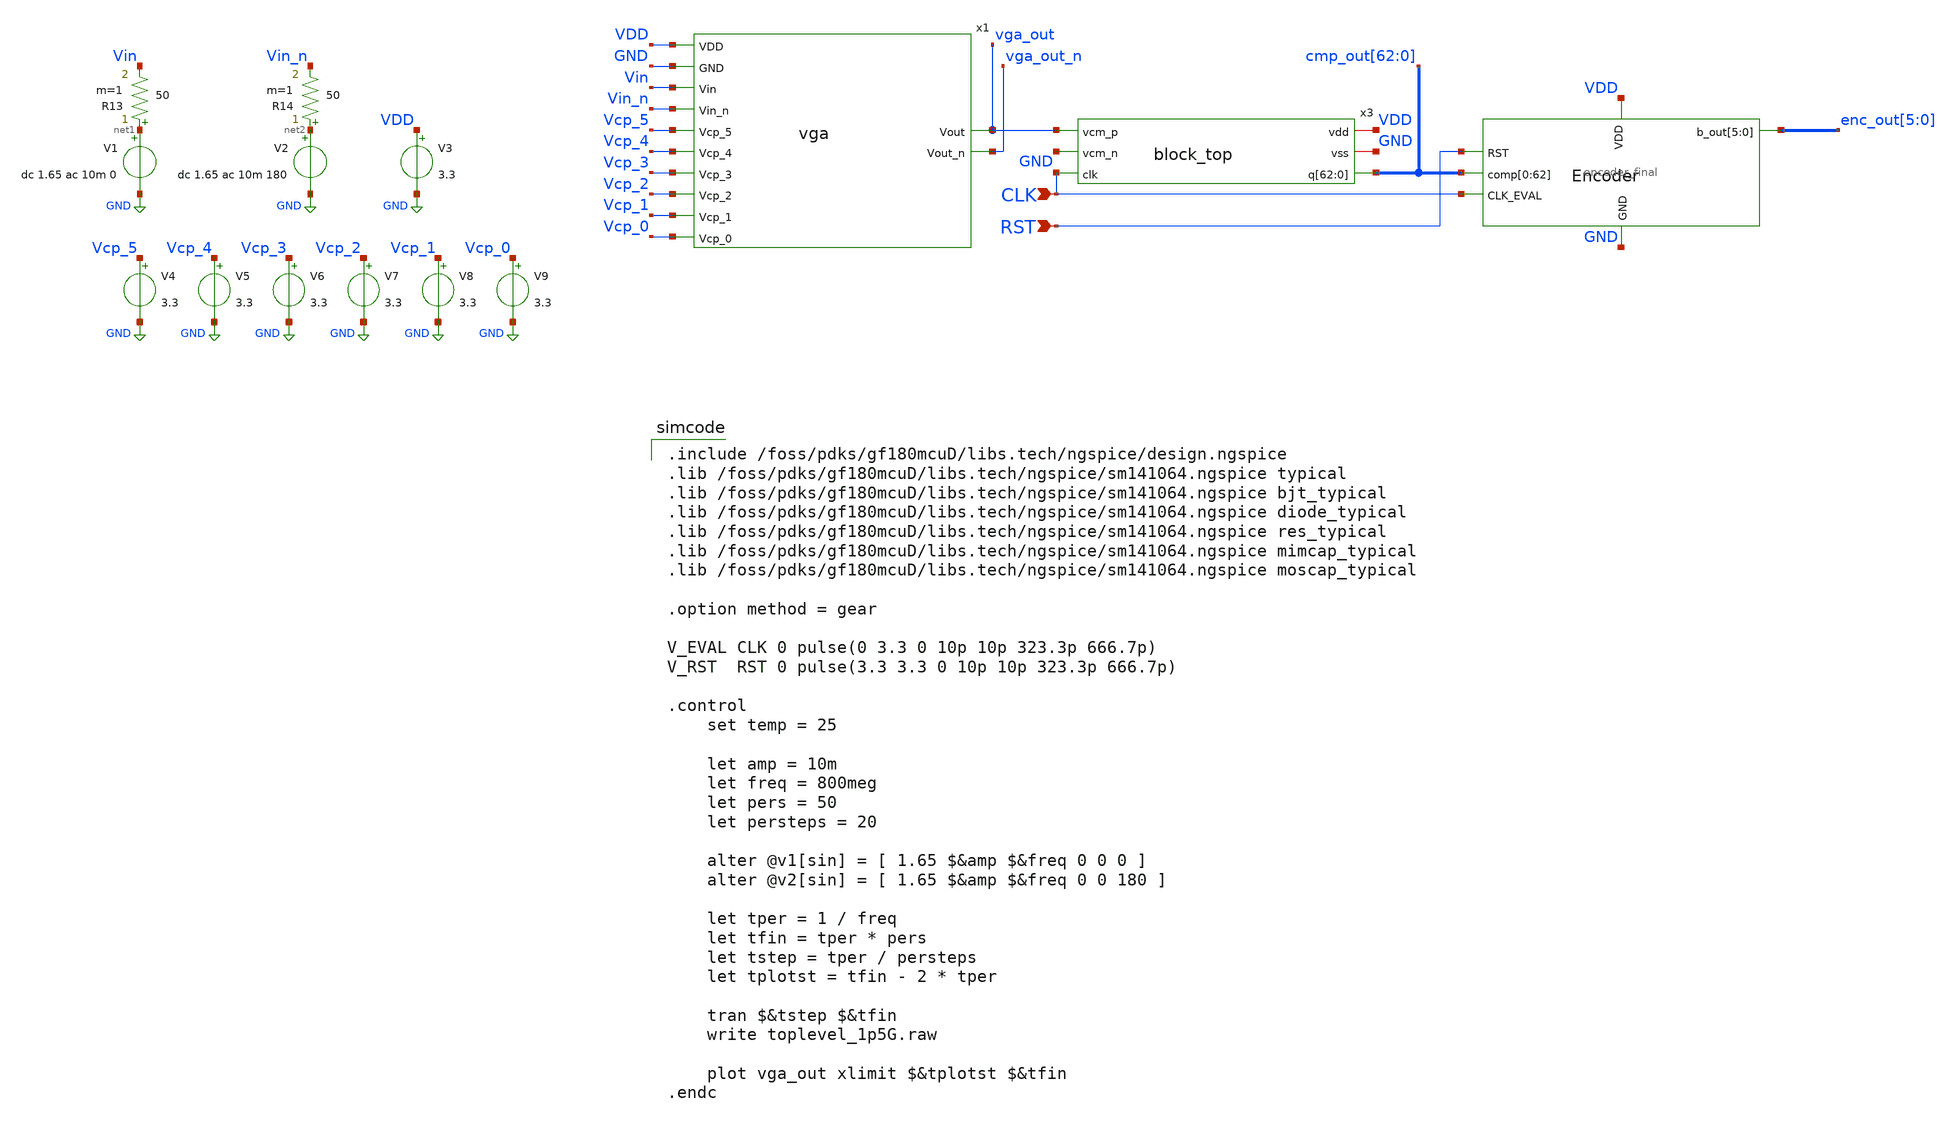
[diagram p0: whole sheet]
** sch_path: blocks/adc/adc_top.sch
**.subckt adc_top CLK RST
*.ipin CLK
*.ipin RST
x1 VDD vga_out Vcp_5 Vcp_4 Vin Vin_n Vcp_2 Vcp_3 Vcp_1 Vcp_0 GND vga_out_n vga
V1 net1 GND dc 1.65 ac 10m 0
V2 net2 GND dc 1.65 ac 10m 180
R14 net2 Vin_n 50 m=1
R13 net1 Vin 50 m=1
V3 VDD GND 3.3
V4 Vcp_5 GND 3.3
V5 Vcp_4 GND 3.3
V6 Vcp_3 GND 3.3
V7 Vcp_2 GND 3.3
V8 Vcp_1 GND 3.3
V9 Vcp_0 GND 3.3
x3 VDD GND vga_out GND CLK cmp_out[62] cmp_out[61] cmp_out[60] cmp_out[59] cmp_out[58] cmp_out[57]
+ cmp_out[56] cmp_out[55] cmp_out[54] cmp_out[53] cmp_out[52] cmp_out[51] cmp_out[50] cmp_out[49] cmp_out[48]
+ cmp_out[47] cmp_out[46] cmp_out[45] cmp_out[44] cmp_out[43] cmp_out[42] cmp_out[41] cmp_out[40] cmp_out[39]
+ cmp_out[38] cmp_out[37] cmp_out[36] cmp_out[35] cmp_out[34] cmp_out[33] cmp_out[32] cmp_out[31] cmp_out[30]
+ cmp_out[29] cmp_out[28] cmp_out[27] cmp_out[26] cmp_out[25] cmp_out[24] cmp_out[23] cmp_out[22] cmp_out[21]
+ cmp_out[20] cmp_out[19] cmp_out[18] cmp_out[17] cmp_out[16] cmp_out[15] cmp_out[14] cmp_out[13] cmp_out[12]
+ cmp_out[11] cmp_out[10] cmp_out[9] cmp_out[8] cmp_out[7] cmp_out[6] cmp_out[5] cmp_out[4] cmp_out[3] cmp_out[2]
+ cmp_out[1] cmp_out[0] block_top
x2 VDD enc_out[5] enc_out[4] enc_out[3] enc_out[2] enc_out[1] enc_out[0] RST cmp_out[62] cmp_out[61]
+ cmp_out[60] cmp_out[59] cmp_out[58] cmp_out[57] cmp_out[56] cmp_out[55] cmp_out[54] cmp_out[53] cmp_out[52]
+ cmp_out[51] cmp_out[50] cmp_out[49] cmp_out[48] cmp_out[47] cmp_out[46] cmp_out[45] cmp_out[44] cmp_out[43]
+ cmp_out[42] cmp_out[41] cmp_out[40] cmp_out[39] cmp_out[38] cmp_out[37] cmp_out[36] cmp_out[35] cmp_out[34]
+ cmp_out[33] cmp_out[32] cmp_out[31] cmp_out[30] cmp_out[29] cmp_out[28] cmp_out[27] cmp_out[26] cmp_out[25]
+ cmp_out[24] cmp_out[23] cmp_out[22] cmp_out[21] cmp_out[20] cmp_out[19] cmp_out[18] cmp_out[17] cmp_out[16]
+ cmp_out[15] cmp_out[14] cmp_out[13] cmp_out[12] cmp_out[11] cmp_out[10] cmp_out[9] cmp_out[8] cmp_out[7]
+ cmp_out[6] cmp_out[5] cmp_out[4] cmp_out[3] cmp_out[2] cmp_out[1] cmp_out[0] CLK GND encoder_final
**** begin user architecture code

.include /foss/pdks/gf180mcuD/libs.tech/ngspice/design.ngspice
.lib /foss/pdks/gf180mcuD/libs.tech/ngspice/sm141064.ngspice typical
.lib /foss/pdks/gf180mcuD/libs.tech/ngspice/sm141064.ngspice bjt_typical
.lib /foss/pdks/gf180mcuD/libs.tech/ngspice/sm141064.ngspice diode_typical
.lib /foss/pdks/gf180mcuD/libs.tech/ngspice/sm141064.ngspice res_typical
.lib /foss/pdks/gf180mcuD/libs.tech/ngspice/sm141064.ngspice mimcap_typical
.lib /foss/pdks/gf180mcuD/libs.tech/ngspice/sm141064.ngspice moscap_typical

.option method = gear

V_EVAL CLK 0 pulse(0 3.3 0 10p 10p 323.3p 666.7p)
V_RST  RST 0 pulse(3.3 3.3 0 10p 10p 323.3p 666.7p)

.control
    set temp = 25

    let amp = 10m
    let freq = 800meg
    let pers = 50
    let persteps = 20

    alter @v1[sin] = [ 1.65 $&amp $&freq 0 0 0 ]
    alter @v2[sin] = [ 1.65 $&amp $&freq 0 0 180 ]

    let tper = 1 / freq
    let tfin = tper * pers
    let tstep = tper / persteps
    let tplotst = tfin - 2 * tper

    tran $&tstep $&tfin
    write toplevel_1p5G.raw

    plot vga_out xlimit $&tplotst $&tfin
.endc


**** end user architecture code
**.ends
.GLOBAL GND
.end
